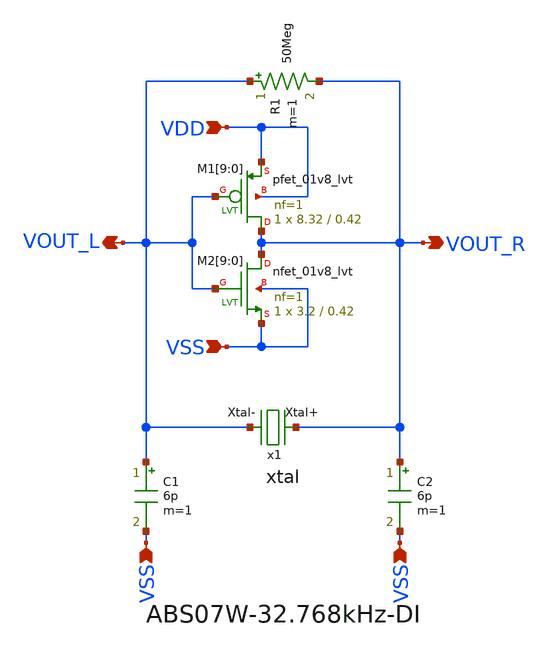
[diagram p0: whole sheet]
** sch_path: design/THESIS_EXP_RO_INVERTER_SKY130A/xtal_osc_schmitt.sch
**.subckt xtal_osc_schmitt VDD VSS VSS VSS VOUT_R VOUT_L
*.ipin VDD
*.ipin VSS
*.ipin VSS
*.ipin VSS
*.opin VOUT_R
*.opin VOUT_L
x1 VOUT_R VOUT_L xtal
C1 VOUT_L VSS 6p m=1
C2 VOUT_R VSS 6p m=1
R1 VOUT_L VOUT_R 50Meg m=1
XM1[9] VOUT_R VOUT_L VDD VDD sky130_fd_pr__pfet_01v8_lvt L=0.42 W=8.32 nf=1 ad='int((nf+1)/2) * W/nf * 0.29'
+ as='int((nf+2)/2) * W/nf * 0.29' pd='2*int((nf+1)/2) * (W/nf + 0.29)' ps='2*int((nf+2)/2) * (W/nf + 0.29)'
+ nrd='0.29 / W' nrs='0.29 / W' sa=0 sb=0 sd=0 mult=1 m=1
XM1[8] VOUT_R VOUT_L VDD VDD sky130_fd_pr__pfet_01v8_lvt L=0.42 W=8.32 nf=1 ad='int((nf+1)/2) * W/nf * 0.29'
+ as='int((nf+2)/2) * W/nf * 0.29' pd='2*int((nf+1)/2) * (W/nf + 0.29)' ps='2*int((nf+2)/2) * (W/nf + 0.29)'
+ nrd='0.29 / W' nrs='0.29 / W' sa=0 sb=0 sd=0 mult=1 m=1
XM1[7] VOUT_R VOUT_L VDD VDD sky130_fd_pr__pfet_01v8_lvt L=0.42 W=8.32 nf=1 ad='int((nf+1)/2) * W/nf * 0.29'
+ as='int((nf+2)/2) * W/nf * 0.29' pd='2*int((nf+1)/2) * (W/nf + 0.29)' ps='2*int((nf+2)/2) * (W/nf + 0.29)'
+ nrd='0.29 / W' nrs='0.29 / W' sa=0 sb=0 sd=0 mult=1 m=1
XM1[6] VOUT_R VOUT_L VDD VDD sky130_fd_pr__pfet_01v8_lvt L=0.42 W=8.32 nf=1 ad='int((nf+1)/2) * W/nf * 0.29'
+ as='int((nf+2)/2) * W/nf * 0.29' pd='2*int((nf+1)/2) * (W/nf + 0.29)' ps='2*int((nf+2)/2) * (W/nf + 0.29)'
+ nrd='0.29 / W' nrs='0.29 / W' sa=0 sb=0 sd=0 mult=1 m=1
XM1[5] VOUT_R VOUT_L VDD VDD sky130_fd_pr__pfet_01v8_lvt L=0.42 W=8.32 nf=1 ad='int((nf+1)/2) * W/nf * 0.29'
+ as='int((nf+2)/2) * W/nf * 0.29' pd='2*int((nf+1)/2) * (W/nf + 0.29)' ps='2*int((nf+2)/2) * (W/nf + 0.29)'
+ nrd='0.29 / W' nrs='0.29 / W' sa=0 sb=0 sd=0 mult=1 m=1
XM1[4] VOUT_R VOUT_L VDD VDD sky130_fd_pr__pfet_01v8_lvt L=0.42 W=8.32 nf=1 ad='int((nf+1)/2) * W/nf * 0.29'
+ as='int((nf+2)/2) * W/nf * 0.29' pd='2*int((nf+1)/2) * (W/nf + 0.29)' ps='2*int((nf+2)/2) * (W/nf + 0.29)'
+ nrd='0.29 / W' nrs='0.29 / W' sa=0 sb=0 sd=0 mult=1 m=1
XM1[3] VOUT_R VOUT_L VDD VDD sky130_fd_pr__pfet_01v8_lvt L=0.42 W=8.32 nf=1 ad='int((nf+1)/2) * W/nf * 0.29'
+ as='int((nf+2)/2) * W/nf * 0.29' pd='2*int((nf+1)/2) * (W/nf + 0.29)' ps='2*int((nf+2)/2) * (W/nf + 0.29)'
+ nrd='0.29 / W' nrs='0.29 / W' sa=0 sb=0 sd=0 mult=1 m=1
XM1[2] VOUT_R VOUT_L VDD VDD sky130_fd_pr__pfet_01v8_lvt L=0.42 W=8.32 nf=1 ad='int((nf+1)/2) * W/nf * 0.29'
+ as='int((nf+2)/2) * W/nf * 0.29' pd='2*int((nf+1)/2) * (W/nf + 0.29)' ps='2*int((nf+2)/2) * (W/nf + 0.29)'
+ nrd='0.29 / W' nrs='0.29 / W' sa=0 sb=0 sd=0 mult=1 m=1
XM1[1] VOUT_R VOUT_L VDD VDD sky130_fd_pr__pfet_01v8_lvt L=0.42 W=8.32 nf=1 ad='int((nf+1)/2) * W/nf * 0.29'
+ as='int((nf+2)/2) * W/nf * 0.29' pd='2*int((nf+1)/2) * (W/nf + 0.29)' ps='2*int((nf+2)/2) * (W/nf + 0.29)'
+ nrd='0.29 / W' nrs='0.29 / W' sa=0 sb=0 sd=0 mult=1 m=1
XM1[0] VOUT_R VOUT_L VDD VDD sky130_fd_pr__pfet_01v8_lvt L=0.42 W=8.32 nf=1 ad='int((nf+1)/2) * W/nf * 0.29'
+ as='int((nf+2)/2) * W/nf * 0.29' pd='2*int((nf+1)/2) * (W/nf + 0.29)' ps='2*int((nf+2)/2) * (W/nf + 0.29)'
+ nrd='0.29 / W' nrs='0.29 / W' sa=0 sb=0 sd=0 mult=1 m=1
XM2[9] VOUT_R VOUT_L VSS VSS sky130_fd_pr__nfet_01v8_lvt L=0.42 W=3.2 nf=1 ad='int((nf+1)/2) * W/nf * 0.29'
+ as='int((nf+2)/2) * W/nf * 0.29' pd='2*int((nf+1)/2) * (W/nf + 0.29)' ps='2*int((nf+2)/2) * (W/nf + 0.29)'
+ nrd='0.29 / W' nrs='0.29 / W' sa=0 sb=0 sd=0 mult=1 m=1
XM2[8] VOUT_R VOUT_L VSS VSS sky130_fd_pr__nfet_01v8_lvt L=0.42 W=3.2 nf=1 ad='int((nf+1)/2) * W/nf * 0.29'
+ as='int((nf+2)/2) * W/nf * 0.29' pd='2*int((nf+1)/2) * (W/nf + 0.29)' ps='2*int((nf+2)/2) * (W/nf + 0.29)'
+ nrd='0.29 / W' nrs='0.29 / W' sa=0 sb=0 sd=0 mult=1 m=1
XM2[7] VOUT_R VOUT_L VSS VSS sky130_fd_pr__nfet_01v8_lvt L=0.42 W=3.2 nf=1 ad='int((nf+1)/2) * W/nf * 0.29'
+ as='int((nf+2)/2) * W/nf * 0.29' pd='2*int((nf+1)/2) * (W/nf + 0.29)' ps='2*int((nf+2)/2) * (W/nf + 0.29)'
+ nrd='0.29 / W' nrs='0.29 / W' sa=0 sb=0 sd=0 mult=1 m=1
XM2[6] VOUT_R VOUT_L VSS VSS sky130_fd_pr__nfet_01v8_lvt L=0.42 W=3.2 nf=1 ad='int((nf+1)/2) * W/nf * 0.29'
+ as='int((nf+2)/2) * W/nf * 0.29' pd='2*int((nf+1)/2) * (W/nf + 0.29)' ps='2*int((nf+2)/2) * (W/nf + 0.29)'
+ nrd='0.29 / W' nrs='0.29 / W' sa=0 sb=0 sd=0 mult=1 m=1
XM2[5] VOUT_R VOUT_L VSS VSS sky130_fd_pr__nfet_01v8_lvt L=0.42 W=3.2 nf=1 ad='int((nf+1)/2) * W/nf * 0.29'
+ as='int((nf+2)/2) * W/nf * 0.29' pd='2*int((nf+1)/2) * (W/nf + 0.29)' ps='2*int((nf+2)/2) * (W/nf + 0.29)'
+ nrd='0.29 / W' nrs='0.29 / W' sa=0 sb=0 sd=0 mult=1 m=1
XM2[4] VOUT_R VOUT_L VSS VSS sky130_fd_pr__nfet_01v8_lvt L=0.42 W=3.2 nf=1 ad='int((nf+1)/2) * W/nf * 0.29'
+ as='int((nf+2)/2) * W/nf * 0.29' pd='2*int((nf+1)/2) * (W/nf + 0.29)' ps='2*int((nf+2)/2) * (W/nf + 0.29)'
+ nrd='0.29 / W' nrs='0.29 / W' sa=0 sb=0 sd=0 mult=1 m=1
XM2[3] VOUT_R VOUT_L VSS VSS sky130_fd_pr__nfet_01v8_lvt L=0.42 W=3.2 nf=1 ad='int((nf+1)/2) * W/nf * 0.29'
+ as='int((nf+2)/2) * W/nf * 0.29' pd='2*int((nf+1)/2) * (W/nf + 0.29)' ps='2*int((nf+2)/2) * (W/nf + 0.29)'
+ nrd='0.29 / W' nrs='0.29 / W' sa=0 sb=0 sd=0 mult=1 m=1
XM2[2] VOUT_R VOUT_L VSS VSS sky130_fd_pr__nfet_01v8_lvt L=0.42 W=3.2 nf=1 ad='int((nf+1)/2) * W/nf * 0.29'
+ as='int((nf+2)/2) * W/nf * 0.29' pd='2*int((nf+1)/2) * (W/nf + 0.29)' ps='2*int((nf+2)/2) * (W/nf + 0.29)'
+ nrd='0.29 / W' nrs='0.29 / W' sa=0 sb=0 sd=0 mult=1 m=1
XM2[1] VOUT_R VOUT_L VSS VSS sky130_fd_pr__nfet_01v8_lvt L=0.42 W=3.2 nf=1 ad='int((nf+1)/2) * W/nf * 0.29'
+ as='int((nf+2)/2) * W/nf * 0.29' pd='2*int((nf+1)/2) * (W/nf + 0.29)' ps='2*int((nf+2)/2) * (W/nf + 0.29)'
+ nrd='0.29 / W' nrs='0.29 / W' sa=0 sb=0 sd=0 mult=1 m=1
XM2[0] VOUT_R VOUT_L VSS VSS sky130_fd_pr__nfet_01v8_lvt L=0.42 W=3.2 nf=1 ad='int((nf+1)/2) * W/nf * 0.29'
+ as='int((nf+2)/2) * W/nf * 0.29' pd='2*int((nf+1)/2) * (W/nf + 0.29)' ps='2*int((nf+2)/2) * (W/nf + 0.29)'
+ nrd='0.29 / W' nrs='0.29 / W' sa=0 sb=0 sd=0 mult=1 m=1
**.ends

* expanding   symbol:  THESIS_EXP_RO_INVERTER_SKY130A/xtal.sym # of pins=2
** sym_path: design/THESIS_EXP_RO_INVERTER_SKY130A/xtal.sym
** sch_path: design/THESIS_EXP_RO_INVERTER_SKY130A/xtal.sch
.subckt xtal Xtal+ Xtal-
*.iopin Xtal+
*.iopin Xtal-
R1 Xtal+ net1 38.194k m=1
C1 net1 net2 4.68f m=1
L1 net2 Xtal- 5048.571 m=1
C2 Xtal+ Xtal- 1.15p m=1
.ends

.end
